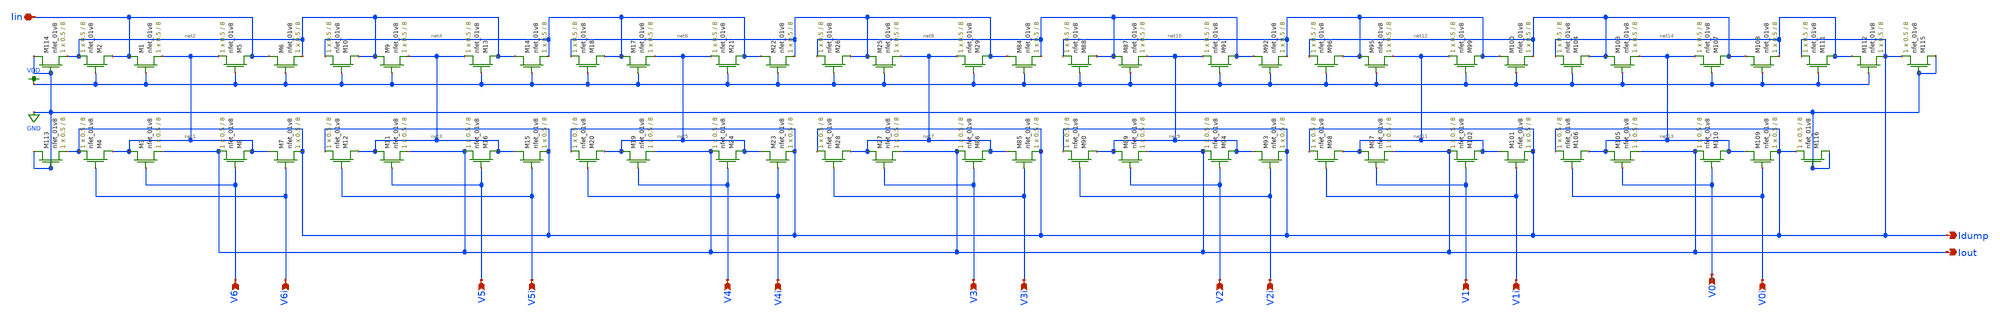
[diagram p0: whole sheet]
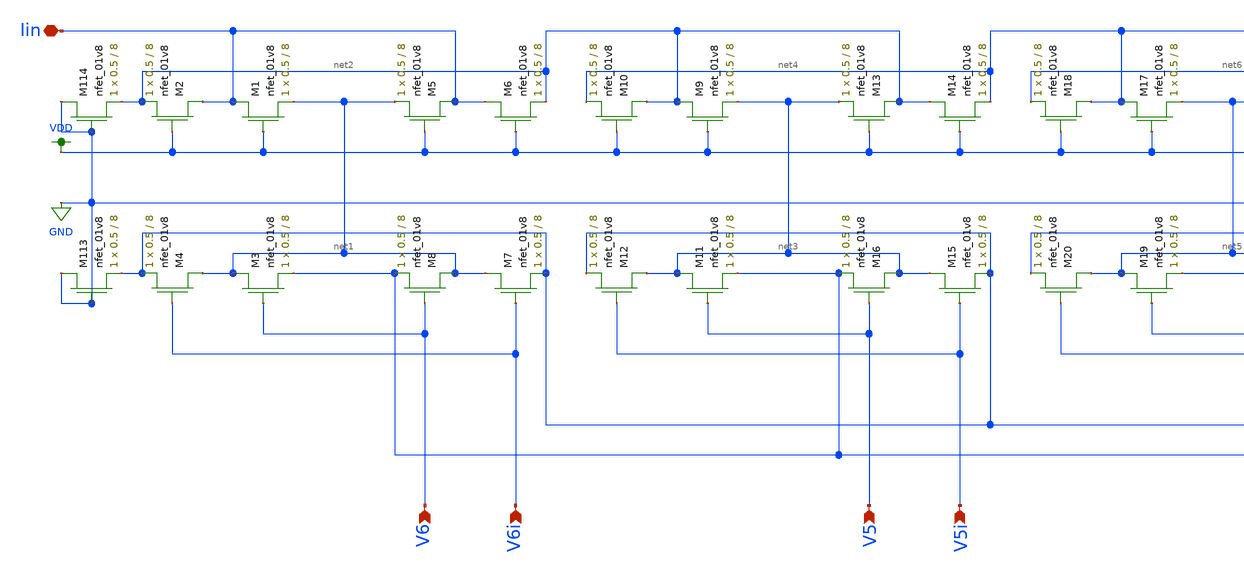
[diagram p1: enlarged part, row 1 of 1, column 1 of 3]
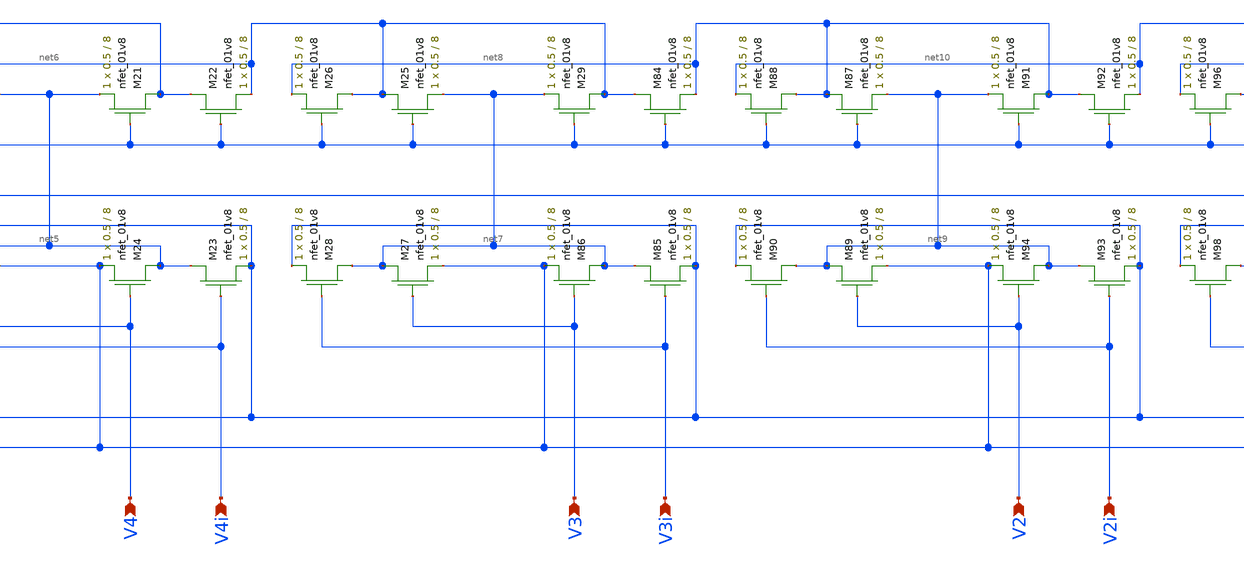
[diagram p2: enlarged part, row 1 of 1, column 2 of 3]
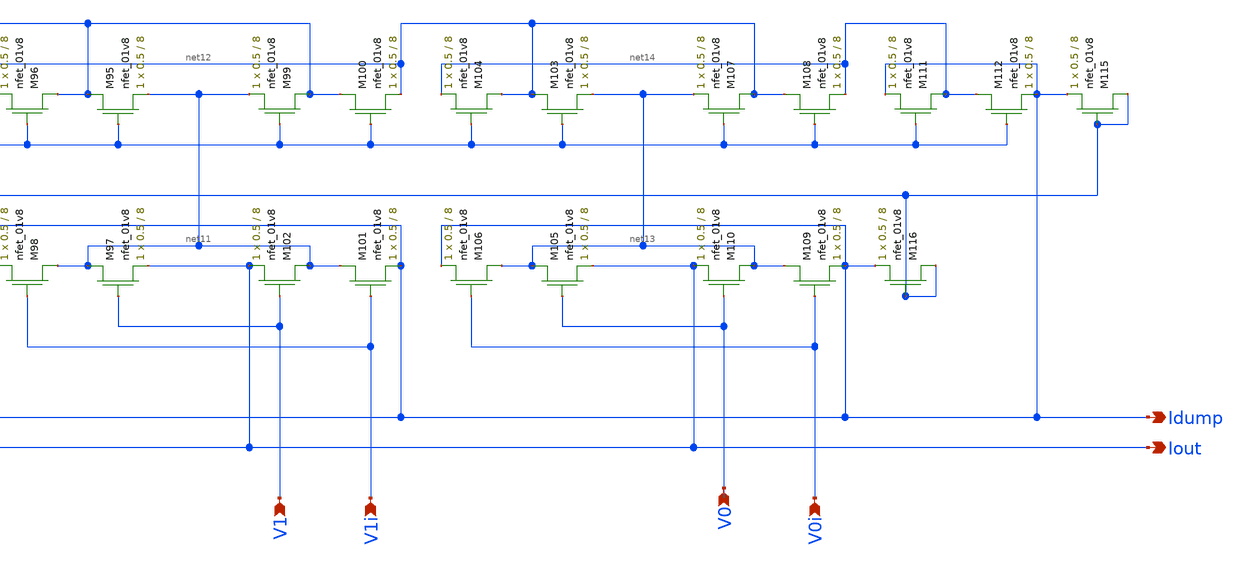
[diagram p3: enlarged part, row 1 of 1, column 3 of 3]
** sch_path: final-final-all/xschem/lds-ladder.sch
**.subckt lds-ladder Iin Idump Iout V6i V5i V4i V3i V2i V1i V0i V6 V5 V4 V3 V2 V1 V0
*.iopin Iin
*.opin Idump
*.opin Iout
*.ipin V6i
*.ipin V5i
*.ipin V4i
*.ipin V3i
*.ipin V2i
*.ipin V1i
*.ipin V0i
*.ipin V6
*.ipin V5
*.ipin V4
*.ipin V3
*.ipin V2
*.ipin V1
*.ipin V0
XM1 Iin VDD net1 GND sky130_fd_pr__nfet_01v8 L=8 W=0.5 nf=1 ad='int((nf+1)/2) * W/nf * 0.29' as='int((nf+2)/2) * W/nf * 0.29'
+ pd='2*int((nf+1)/2) * (W/nf + 0.29)' ps='2*int((nf+2)/2) * (W/nf + 0.29)' nrd='0.29 / W' nrs='0.29 / W'
+ sa=0 sb=0 sd=0 mult=1 m=1
XM2 Iin VDD net2 GND sky130_fd_pr__nfet_01v8 L=8 W=0.5 nf=1 ad='int((nf+1)/2) * W/nf * 0.29' as='int((nf+2)/2) * W/nf * 0.29'
+ pd='2*int((nf+1)/2) * (W/nf + 0.29)' ps='2*int((nf+2)/2) * (W/nf + 0.29)' nrd='0.29 / W' nrs='0.29 / W'
+ sa=0 sb=0 sd=0 mult=1 m=1
XM3 net1 V6 Iout GND sky130_fd_pr__nfet_01v8 L=8 W=0.5 nf=1 ad='int((nf+1)/2) * W/nf * 0.29' as='int((nf+2)/2) * W/nf * 0.29'
+ pd='2*int((nf+1)/2) * (W/nf + 0.29)' ps='2*int((nf+2)/2) * (W/nf + 0.29)' nrd='0.29 / W' nrs='0.29 / W'
+ sa=0 sb=0 sd=0 mult=1 m=1
XM4 net1 V6i Idump GND sky130_fd_pr__nfet_01v8 L=8 W=0.5 nf=1 ad='int((nf+1)/2) * W/nf * 0.29' as='int((nf+2)/2) * W/nf * 0.29'
+ pd='2*int((nf+1)/2) * (W/nf + 0.29)' ps='2*int((nf+2)/2) * (W/nf + 0.29)' nrd='0.29 / W' nrs='0.29 / W'
+ sa=0 sb=0 sd=0 mult=1 m=1
XM5 Iin VDD net1 GND sky130_fd_pr__nfet_01v8 L=8 W=0.5 nf=1 ad='int((nf+1)/2) * W/nf * 0.29' as='int((nf+2)/2) * W/nf * 0.29'
+ pd='2*int((nf+1)/2) * (W/nf + 0.29)' ps='2*int((nf+2)/2) * (W/nf + 0.29)' nrd='0.29 / W' nrs='0.29 / W'
+ sa=0 sb=0 sd=0 mult=1 m=1
XM6 Iin VDD net2 GND sky130_fd_pr__nfet_01v8 L=8 W=0.5 nf=1 ad='int((nf+1)/2) * W/nf * 0.29' as='int((nf+2)/2) * W/nf * 0.29'
+ pd='2*int((nf+1)/2) * (W/nf + 0.29)' ps='2*int((nf+2)/2) * (W/nf + 0.29)' nrd='0.29 / W' nrs='0.29 / W'
+ sa=0 sb=0 sd=0 mult=1 m=1
XM7 net1 V6i Idump GND sky130_fd_pr__nfet_01v8 L=8 W=0.5 nf=1 ad='int((nf+1)/2) * W/nf * 0.29' as='int((nf+2)/2) * W/nf * 0.29'
+ pd='2*int((nf+1)/2) * (W/nf + 0.29)' ps='2*int((nf+2)/2) * (W/nf + 0.29)' nrd='0.29 / W' nrs='0.29 / W'
+ sa=0 sb=0 sd=0 mult=1 m=1
XM8 net1 V6 Iout GND sky130_fd_pr__nfet_01v8 L=8 W=0.5 nf=1 ad='int((nf+1)/2) * W/nf * 0.29' as='int((nf+2)/2) * W/nf * 0.29'
+ pd='2*int((nf+1)/2) * (W/nf + 0.29)' ps='2*int((nf+2)/2) * (W/nf + 0.29)' nrd='0.29 / W' nrs='0.29 / W'
+ sa=0 sb=0 sd=0 mult=1 m=1
XM9 net2 VDD net3 GND sky130_fd_pr__nfet_01v8 L=8 W=0.5 nf=1 ad='int((nf+1)/2) * W/nf * 0.29' as='int((nf+2)/2) * W/nf * 0.29'
+ pd='2*int((nf+1)/2) * (W/nf + 0.29)' ps='2*int((nf+2)/2) * (W/nf + 0.29)' nrd='0.29 / W' nrs='0.29 / W'
+ sa=0 sb=0 sd=0 mult=1 m=1
XM10 net2 VDD net4 GND sky130_fd_pr__nfet_01v8 L=8 W=0.5 nf=1 ad='int((nf+1)/2) * W/nf * 0.29' as='int((nf+2)/2) * W/nf * 0.29'
+ pd='2*int((nf+1)/2) * (W/nf + 0.29)' ps='2*int((nf+2)/2) * (W/nf + 0.29)' nrd='0.29 / W' nrs='0.29 / W'
+ sa=0 sb=0 sd=0 mult=1 m=1
XM11 net3 V5 Iout GND sky130_fd_pr__nfet_01v8 L=8 W=0.5 nf=1 ad='int((nf+1)/2) * W/nf * 0.29' as='int((nf+2)/2) * W/nf * 0.29'
+ pd='2*int((nf+1)/2) * (W/nf + 0.29)' ps='2*int((nf+2)/2) * (W/nf + 0.29)' nrd='0.29 / W' nrs='0.29 / W'
+ sa=0 sb=0 sd=0 mult=1 m=1
XM12 net3 V5i Idump GND sky130_fd_pr__nfet_01v8 L=8 W=0.5 nf=1 ad='int((nf+1)/2) * W/nf * 0.29' as='int((nf+2)/2) * W/nf * 0.29'
+ pd='2*int((nf+1)/2) * (W/nf + 0.29)' ps='2*int((nf+2)/2) * (W/nf + 0.29)' nrd='0.29 / W' nrs='0.29 / W'
+ sa=0 sb=0 sd=0 mult=1 m=1
XM13 net2 VDD net3 GND sky130_fd_pr__nfet_01v8 L=8 W=0.5 nf=1 ad='int((nf+1)/2) * W/nf * 0.29' as='int((nf+2)/2) * W/nf * 0.29'
+ pd='2*int((nf+1)/2) * (W/nf + 0.29)' ps='2*int((nf+2)/2) * (W/nf + 0.29)' nrd='0.29 / W' nrs='0.29 / W'
+ sa=0 sb=0 sd=0 mult=1 m=1
XM14 net2 VDD net4 GND sky130_fd_pr__nfet_01v8 L=8 W=0.5 nf=1 ad='int((nf+1)/2) * W/nf * 0.29' as='int((nf+2)/2) * W/nf * 0.29'
+ pd='2*int((nf+1)/2) * (W/nf + 0.29)' ps='2*int((nf+2)/2) * (W/nf + 0.29)' nrd='0.29 / W' nrs='0.29 / W'
+ sa=0 sb=0 sd=0 mult=1 m=1
XM15 net3 V5i Idump GND sky130_fd_pr__nfet_01v8 L=8 W=0.5 nf=1 ad='int((nf+1)/2) * W/nf * 0.29' as='int((nf+2)/2) * W/nf * 0.29'
+ pd='2*int((nf+1)/2) * (W/nf + 0.29)' ps='2*int((nf+2)/2) * (W/nf + 0.29)' nrd='0.29 / W' nrs='0.29 / W'
+ sa=0 sb=0 sd=0 mult=1 m=1
XM16 net3 V5 Iout GND sky130_fd_pr__nfet_01v8 L=8 W=0.5 nf=1 ad='int((nf+1)/2) * W/nf * 0.29' as='int((nf+2)/2) * W/nf * 0.29'
+ pd='2*int((nf+1)/2) * (W/nf + 0.29)' ps='2*int((nf+2)/2) * (W/nf + 0.29)' nrd='0.29 / W' nrs='0.29 / W'
+ sa=0 sb=0 sd=0 mult=1 m=1
XM17 net4 VDD net5 GND sky130_fd_pr__nfet_01v8 L=8 W=0.5 nf=1 ad='int((nf+1)/2) * W/nf * 0.29' as='int((nf+2)/2) * W/nf * 0.29'
+ pd='2*int((nf+1)/2) * (W/nf + 0.29)' ps='2*int((nf+2)/2) * (W/nf + 0.29)' nrd='0.29 / W' nrs='0.29 / W'
+ sa=0 sb=0 sd=0 mult=1 m=1
XM18 net4 VDD net6 GND sky130_fd_pr__nfet_01v8 L=8 W=0.5 nf=1 ad='int((nf+1)/2) * W/nf * 0.29' as='int((nf+2)/2) * W/nf * 0.29'
+ pd='2*int((nf+1)/2) * (W/nf + 0.29)' ps='2*int((nf+2)/2) * (W/nf + 0.29)' nrd='0.29 / W' nrs='0.29 / W'
+ sa=0 sb=0 sd=0 mult=1 m=1
XM19 net5 V4 Iout GND sky130_fd_pr__nfet_01v8 L=8 W=0.5 nf=1 ad='int((nf+1)/2) * W/nf * 0.29' as='int((nf+2)/2) * W/nf * 0.29'
+ pd='2*int((nf+1)/2) * (W/nf + 0.29)' ps='2*int((nf+2)/2) * (W/nf + 0.29)' nrd='0.29 / W' nrs='0.29 / W'
+ sa=0 sb=0 sd=0 mult=1 m=1
XM20 net5 V4i Idump GND sky130_fd_pr__nfet_01v8 L=8 W=0.5 nf=1 ad='int((nf+1)/2) * W/nf * 0.29' as='int((nf+2)/2) * W/nf * 0.29'
+ pd='2*int((nf+1)/2) * (W/nf + 0.29)' ps='2*int((nf+2)/2) * (W/nf + 0.29)' nrd='0.29 / W' nrs='0.29 / W'
+ sa=0 sb=0 sd=0 mult=1 m=1
XM21 net4 VDD net5 GND sky130_fd_pr__nfet_01v8 L=8 W=0.5 nf=1 ad='int((nf+1)/2) * W/nf * 0.29' as='int((nf+2)/2) * W/nf * 0.29'
+ pd='2*int((nf+1)/2) * (W/nf + 0.29)' ps='2*int((nf+2)/2) * (W/nf + 0.29)' nrd='0.29 / W' nrs='0.29 / W'
+ sa=0 sb=0 sd=0 mult=1 m=1
XM22 net4 VDD net6 GND sky130_fd_pr__nfet_01v8 L=8 W=0.5 nf=1 ad='int((nf+1)/2) * W/nf * 0.29' as='int((nf+2)/2) * W/nf * 0.29'
+ pd='2*int((nf+1)/2) * (W/nf + 0.29)' ps='2*int((nf+2)/2) * (W/nf + 0.29)' nrd='0.29 / W' nrs='0.29 / W'
+ sa=0 sb=0 sd=0 mult=1 m=1
XM23 net5 V4i Idump GND sky130_fd_pr__nfet_01v8 L=8 W=0.5 nf=1 ad='int((nf+1)/2) * W/nf * 0.29' as='int((nf+2)/2) * W/nf * 0.29'
+ pd='2*int((nf+1)/2) * (W/nf + 0.29)' ps='2*int((nf+2)/2) * (W/nf + 0.29)' nrd='0.29 / W' nrs='0.29 / W'
+ sa=0 sb=0 sd=0 mult=1 m=1
XM24 net5 V4 Iout GND sky130_fd_pr__nfet_01v8 L=8 W=0.5 nf=1 ad='int((nf+1)/2) * W/nf * 0.29' as='int((nf+2)/2) * W/nf * 0.29'
+ pd='2*int((nf+1)/2) * (W/nf + 0.29)' ps='2*int((nf+2)/2) * (W/nf + 0.29)' nrd='0.29 / W' nrs='0.29 / W'
+ sa=0 sb=0 sd=0 mult=1 m=1
XM25 net6 VDD net7 GND sky130_fd_pr__nfet_01v8 L=8 W=0.5 nf=1 ad='int((nf+1)/2) * W/nf * 0.29' as='int((nf+2)/2) * W/nf * 0.29'
+ pd='2*int((nf+1)/2) * (W/nf + 0.29)' ps='2*int((nf+2)/2) * (W/nf + 0.29)' nrd='0.29 / W' nrs='0.29 / W'
+ sa=0 sb=0 sd=0 mult=1 m=1
XM26 net6 VDD net8 GND sky130_fd_pr__nfet_01v8 L=8 W=0.5 nf=1 ad='int((nf+1)/2) * W/nf * 0.29' as='int((nf+2)/2) * W/nf * 0.29'
+ pd='2*int((nf+1)/2) * (W/nf + 0.29)' ps='2*int((nf+2)/2) * (W/nf + 0.29)' nrd='0.29 / W' nrs='0.29 / W'
+ sa=0 sb=0 sd=0 mult=1 m=1
XM27 net7 V3 Iout GND sky130_fd_pr__nfet_01v8 L=8 W=0.5 nf=1 ad='int((nf+1)/2) * W/nf * 0.29' as='int((nf+2)/2) * W/nf * 0.29'
+ pd='2*int((nf+1)/2) * (W/nf + 0.29)' ps='2*int((nf+2)/2) * (W/nf + 0.29)' nrd='0.29 / W' nrs='0.29 / W'
+ sa=0 sb=0 sd=0 mult=1 m=1
XM28 net7 V3i Idump GND sky130_fd_pr__nfet_01v8 L=8 W=0.5 nf=1 ad='int((nf+1)/2) * W/nf * 0.29' as='int((nf+2)/2) * W/nf * 0.29'
+ pd='2*int((nf+1)/2) * (W/nf + 0.29)' ps='2*int((nf+2)/2) * (W/nf + 0.29)' nrd='0.29 / W' nrs='0.29 / W'
+ sa=0 sb=0 sd=0 mult=1 m=1
XM29 net6 VDD net7 GND sky130_fd_pr__nfet_01v8 L=8 W=0.5 nf=1 ad='int((nf+1)/2) * W/nf * 0.29' as='int((nf+2)/2) * W/nf * 0.29'
+ pd='2*int((nf+1)/2) * (W/nf + 0.29)' ps='2*int((nf+2)/2) * (W/nf + 0.29)' nrd='0.29 / W' nrs='0.29 / W'
+ sa=0 sb=0 sd=0 mult=1 m=1
XM84 net6 VDD net8 GND sky130_fd_pr__nfet_01v8 L=8 W=0.5 nf=1 ad='int((nf+1)/2) * W/nf * 0.29' as='int((nf+2)/2) * W/nf * 0.29'
+ pd='2*int((nf+1)/2) * (W/nf + 0.29)' ps='2*int((nf+2)/2) * (W/nf + 0.29)' nrd='0.29 / W' nrs='0.29 / W'
+ sa=0 sb=0 sd=0 mult=1 m=1
XM85 net7 V3i Idump GND sky130_fd_pr__nfet_01v8 L=8 W=0.5 nf=1 ad='int((nf+1)/2) * W/nf * 0.29' as='int((nf+2)/2) * W/nf * 0.29'
+ pd='2*int((nf+1)/2) * (W/nf + 0.29)' ps='2*int((nf+2)/2) * (W/nf + 0.29)' nrd='0.29 / W' nrs='0.29 / W'
+ sa=0 sb=0 sd=0 mult=1 m=1
XM86 net7 V3 Iout GND sky130_fd_pr__nfet_01v8 L=8 W=0.5 nf=1 ad='int((nf+1)/2) * W/nf * 0.29' as='int((nf+2)/2) * W/nf * 0.29'
+ pd='2*int((nf+1)/2) * (W/nf + 0.29)' ps='2*int((nf+2)/2) * (W/nf + 0.29)' nrd='0.29 / W' nrs='0.29 / W'
+ sa=0 sb=0 sd=0 mult=1 m=1
XM87 net8 VDD net9 GND sky130_fd_pr__nfet_01v8 L=8 W=0.5 nf=1 ad='int((nf+1)/2) * W/nf * 0.29' as='int((nf+2)/2) * W/nf * 0.29'
+ pd='2*int((nf+1)/2) * (W/nf + 0.29)' ps='2*int((nf+2)/2) * (W/nf + 0.29)' nrd='0.29 / W' nrs='0.29 / W'
+ sa=0 sb=0 sd=0 mult=1 m=1
XM88 net8 VDD net10 GND sky130_fd_pr__nfet_01v8 L=8 W=0.5 nf=1 ad='int((nf+1)/2) * W/nf * 0.29' as='int((nf+2)/2) * W/nf * 0.29'
+ pd='2*int((nf+1)/2) * (W/nf + 0.29)' ps='2*int((nf+2)/2) * (W/nf + 0.29)' nrd='0.29 / W' nrs='0.29 / W'
+ sa=0 sb=0 sd=0 mult=1 m=1
XM89 net9 V2 Iout GND sky130_fd_pr__nfet_01v8 L=8 W=0.5 nf=1 ad='int((nf+1)/2) * W/nf * 0.29' as='int((nf+2)/2) * W/nf * 0.29'
+ pd='2*int((nf+1)/2) * (W/nf + 0.29)' ps='2*int((nf+2)/2) * (W/nf + 0.29)' nrd='0.29 / W' nrs='0.29 / W'
+ sa=0 sb=0 sd=0 mult=1 m=1
XM90 net9 V2i Idump GND sky130_fd_pr__nfet_01v8 L=8 W=0.5 nf=1 ad='int((nf+1)/2) * W/nf * 0.29' as='int((nf+2)/2) * W/nf * 0.29'
+ pd='2*int((nf+1)/2) * (W/nf + 0.29)' ps='2*int((nf+2)/2) * (W/nf + 0.29)' nrd='0.29 / W' nrs='0.29 / W'
+ sa=0 sb=0 sd=0 mult=1 m=1
XM91 net8 VDD net9 GND sky130_fd_pr__nfet_01v8 L=8 W=0.5 nf=1 ad='int((nf+1)/2) * W/nf * 0.29' as='int((nf+2)/2) * W/nf * 0.29'
+ pd='2*int((nf+1)/2) * (W/nf + 0.29)' ps='2*int((nf+2)/2) * (W/nf + 0.29)' nrd='0.29 / W' nrs='0.29 / W'
+ sa=0 sb=0 sd=0 mult=1 m=1
XM92 net8 VDD net10 GND sky130_fd_pr__nfet_01v8 L=8 W=0.5 nf=1 ad='int((nf+1)/2) * W/nf * 0.29' as='int((nf+2)/2) * W/nf * 0.29'
+ pd='2*int((nf+1)/2) * (W/nf + 0.29)' ps='2*int((nf+2)/2) * (W/nf + 0.29)' nrd='0.29 / W' nrs='0.29 / W'
+ sa=0 sb=0 sd=0 mult=1 m=1
XM93 net9 V2i Idump GND sky130_fd_pr__nfet_01v8 L=8 W=0.5 nf=1 ad='int((nf+1)/2) * W/nf * 0.29' as='int((nf+2)/2) * W/nf * 0.29'
+ pd='2*int((nf+1)/2) * (W/nf + 0.29)' ps='2*int((nf+2)/2) * (W/nf + 0.29)' nrd='0.29 / W' nrs='0.29 / W'
+ sa=0 sb=0 sd=0 mult=1 m=1
XM94 net9 V2 Iout GND sky130_fd_pr__nfet_01v8 L=8 W=0.5 nf=1 ad='int((nf+1)/2) * W/nf * 0.29' as='int((nf+2)/2) * W/nf * 0.29'
+ pd='2*int((nf+1)/2) * (W/nf + 0.29)' ps='2*int((nf+2)/2) * (W/nf + 0.29)' nrd='0.29 / W' nrs='0.29 / W'
+ sa=0 sb=0 sd=0 mult=1 m=1
XM95 net10 VDD net11 GND sky130_fd_pr__nfet_01v8 L=8 W=0.5 nf=1 ad='int((nf+1)/2) * W/nf * 0.29' as='int((nf+2)/2) * W/nf * 0.29'
+ pd='2*int((nf+1)/2) * (W/nf + 0.29)' ps='2*int((nf+2)/2) * (W/nf + 0.29)' nrd='0.29 / W' nrs='0.29 / W'
+ sa=0 sb=0 sd=0 mult=1 m=1
XM96 net10 VDD net12 GND sky130_fd_pr__nfet_01v8 L=8 W=0.5 nf=1 ad='int((nf+1)/2) * W/nf * 0.29' as='int((nf+2)/2) * W/nf * 0.29'
+ pd='2*int((nf+1)/2) * (W/nf + 0.29)' ps='2*int((nf+2)/2) * (W/nf + 0.29)' nrd='0.29 / W' nrs='0.29 / W'
+ sa=0 sb=0 sd=0 mult=1 m=1
XM97 net11 V1 Iout GND sky130_fd_pr__nfet_01v8 L=8 W=0.5 nf=1 ad='int((nf+1)/2) * W/nf * 0.29' as='int((nf+2)/2) * W/nf * 0.29'
+ pd='2*int((nf+1)/2) * (W/nf + 0.29)' ps='2*int((nf+2)/2) * (W/nf + 0.29)' nrd='0.29 / W' nrs='0.29 / W'
+ sa=0 sb=0 sd=0 mult=1 m=1
XM98 net11 V1i Idump GND sky130_fd_pr__nfet_01v8 L=8 W=0.5 nf=1 ad='int((nf+1)/2) * W/nf * 0.29' as='int((nf+2)/2) * W/nf * 0.29'
+ pd='2*int((nf+1)/2) * (W/nf + 0.29)' ps='2*int((nf+2)/2) * (W/nf + 0.29)' nrd='0.29 / W' nrs='0.29 / W'
+ sa=0 sb=0 sd=0 mult=1 m=1
XM99 net10 VDD net11 GND sky130_fd_pr__nfet_01v8 L=8 W=0.5 nf=1 ad='int((nf+1)/2) * W/nf * 0.29' as='int((nf+2)/2) * W/nf * 0.29'
+ pd='2*int((nf+1)/2) * (W/nf + 0.29)' ps='2*int((nf+2)/2) * (W/nf + 0.29)' nrd='0.29 / W' nrs='0.29 / W'
+ sa=0 sb=0 sd=0 mult=1 m=1
XM100 net10 VDD net12 GND sky130_fd_pr__nfet_01v8 L=8 W=0.5 nf=1 ad='int((nf+1)/2) * W/nf * 0.29' as='int((nf+2)/2) * W/nf * 0.29'
+ pd='2*int((nf+1)/2) * (W/nf + 0.29)' ps='2*int((nf+2)/2) * (W/nf + 0.29)' nrd='0.29 / W' nrs='0.29 / W'
+ sa=0 sb=0 sd=0 mult=1 m=1
XM101 net11 V1i Idump GND sky130_fd_pr__nfet_01v8 L=8 W=0.5 nf=1 ad='int((nf+1)/2) * W/nf * 0.29' as='int((nf+2)/2) * W/nf * 0.29'
+ pd='2*int((nf+1)/2) * (W/nf + 0.29)' ps='2*int((nf+2)/2) * (W/nf + 0.29)' nrd='0.29 / W' nrs='0.29 / W'
+ sa=0 sb=0 sd=0 mult=1 m=1
XM102 net11 V1 Iout GND sky130_fd_pr__nfet_01v8 L=8 W=0.5 nf=1 ad='int((nf+1)/2) * W/nf * 0.29' as='int((nf+2)/2) * W/nf * 0.29'
+ pd='2*int((nf+1)/2) * (W/nf + 0.29)' ps='2*int((nf+2)/2) * (W/nf + 0.29)' nrd='0.29 / W' nrs='0.29 / W'
+ sa=0 sb=0 sd=0 mult=1 m=1
XM103 net12 VDD net13 GND sky130_fd_pr__nfet_01v8 L=8 W=0.5 nf=1 ad='int((nf+1)/2) * W/nf * 0.29' as='int((nf+2)/2) * W/nf * 0.29'
+ pd='2*int((nf+1)/2) * (W/nf + 0.29)' ps='2*int((nf+2)/2) * (W/nf + 0.29)' nrd='0.29 / W' nrs='0.29 / W'
+ sa=0 sb=0 sd=0 mult=1 m=1
XM104 net12 VDD net14 GND sky130_fd_pr__nfet_01v8 L=8 W=0.5 nf=1 ad='int((nf+1)/2) * W/nf * 0.29' as='int((nf+2)/2) * W/nf * 0.29'
+ pd='2*int((nf+1)/2) * (W/nf + 0.29)' ps='2*int((nf+2)/2) * (W/nf + 0.29)' nrd='0.29 / W' nrs='0.29 / W'
+ sa=0 sb=0 sd=0 mult=1 m=1
XM105 net13 V0 Iout GND sky130_fd_pr__nfet_01v8 L=8 W=0.5 nf=1 ad='int((nf+1)/2) * W/nf * 0.29' as='int((nf+2)/2) * W/nf * 0.29'
+ pd='2*int((nf+1)/2) * (W/nf + 0.29)' ps='2*int((nf+2)/2) * (W/nf + 0.29)' nrd='0.29 / W' nrs='0.29 / W'
+ sa=0 sb=0 sd=0 mult=1 m=1
XM106 net13 V0i Idump GND sky130_fd_pr__nfet_01v8 L=8 W=0.5 nf=1 ad='int((nf+1)/2) * W/nf * 0.29' as='int((nf+2)/2) * W/nf * 0.29'
+ pd='2*int((nf+1)/2) * (W/nf + 0.29)' ps='2*int((nf+2)/2) * (W/nf + 0.29)' nrd='0.29 / W' nrs='0.29 / W'
+ sa=0 sb=0 sd=0 mult=1 m=1
XM107 net12 VDD net13 GND sky130_fd_pr__nfet_01v8 L=8 W=0.5 nf=1 ad='int((nf+1)/2) * W/nf * 0.29' as='int((nf+2)/2) * W/nf * 0.29'
+ pd='2*int((nf+1)/2) * (W/nf + 0.29)' ps='2*int((nf+2)/2) * (W/nf + 0.29)' nrd='0.29 / W' nrs='0.29 / W'
+ sa=0 sb=0 sd=0 mult=1 m=1
XM108 net12 VDD net14 GND sky130_fd_pr__nfet_01v8 L=8 W=0.5 nf=1 ad='int((nf+1)/2) * W/nf * 0.29' as='int((nf+2)/2) * W/nf * 0.29'
+ pd='2*int((nf+1)/2) * (W/nf + 0.29)' ps='2*int((nf+2)/2) * (W/nf + 0.29)' nrd='0.29 / W' nrs='0.29 / W'
+ sa=0 sb=0 sd=0 mult=1 m=1
XM109 net13 V0i Idump GND sky130_fd_pr__nfet_01v8 L=8 W=0.5 nf=1 ad='int((nf+1)/2) * W/nf * 0.29' as='int((nf+2)/2) * W/nf * 0.29'
+ pd='2*int((nf+1)/2) * (W/nf + 0.29)' ps='2*int((nf+2)/2) * (W/nf + 0.29)' nrd='0.29 / W' nrs='0.29 / W'
+ sa=0 sb=0 sd=0 mult=1 m=1
XM110 net13 V0 Iout GND sky130_fd_pr__nfet_01v8 L=8 W=0.5 nf=1 ad='int((nf+1)/2) * W/nf * 0.29' as='int((nf+2)/2) * W/nf * 0.29'
+ pd='2*int((nf+1)/2) * (W/nf + 0.29)' ps='2*int((nf+2)/2) * (W/nf + 0.29)' nrd='0.29 / W' nrs='0.29 / W'
+ sa=0 sb=0 sd=0 mult=1 m=1
XM111 net14 VDD Idump GND sky130_fd_pr__nfet_01v8 L=8 W=0.5 nf=1 ad='int((nf+1)/2) * W/nf * 0.29' as='int((nf+2)/2) * W/nf * 0.29'
+ pd='2*int((nf+1)/2) * (W/nf + 0.29)' ps='2*int((nf+2)/2) * (W/nf + 0.29)' nrd='0.29 / W' nrs='0.29 / W'
+ sa=0 sb=0 sd=0 mult=1 m=1
XM112 net14 VDD Idump GND sky130_fd_pr__nfet_01v8 L=8 W=0.5 nf=1 ad='int((nf+1)/2) * W/nf * 0.29' as='int((nf+2)/2) * W/nf * 0.29'
+ pd='2*int((nf+1)/2) * (W/nf + 0.29)' ps='2*int((nf+2)/2) * (W/nf + 0.29)' nrd='0.29 / W' nrs='0.29 / W'
+ sa=0 sb=0 sd=0 mult=1 m=1
XM113 GND GND Idump GND sky130_fd_pr__nfet_01v8 L=8 W=0.5 nf=1 ad='int((nf+1)/2) * W/nf * 0.29' as='int((nf+2)/2) * W/nf * 0.29'
+ pd='2*int((nf+1)/2) * (W/nf + 0.29)' ps='2*int((nf+2)/2) * (W/nf + 0.29)' nrd='0.29 / W' nrs='0.29 / W'
+ sa=0 sb=0 sd=0 mult=1 m=1
XM114 GND GND net2 GND sky130_fd_pr__nfet_01v8 L=8 W=0.5 nf=1 ad='int((nf+1)/2) * W/nf * 0.29' as='int((nf+2)/2) * W/nf * 0.29'
+ pd='2*int((nf+1)/2) * (W/nf + 0.29)' ps='2*int((nf+2)/2) * (W/nf + 0.29)' nrd='0.29 / W' nrs='0.29 / W'
+ sa=0 sb=0 sd=0 mult=1 m=1
XM115 GND GND Idump GND sky130_fd_pr__nfet_01v8 L=8 W=0.5 nf=1 ad='int((nf+1)/2) * W/nf * 0.29' as='int((nf+2)/2) * W/nf * 0.29'
+ pd='2*int((nf+1)/2) * (W/nf + 0.29)' ps='2*int((nf+2)/2) * (W/nf + 0.29)' nrd='0.29 / W' nrs='0.29 / W'
+ sa=0 sb=0 sd=0 mult=1 m=1
XM116 GND GND Idump GND sky130_fd_pr__nfet_01v8 L=8 W=0.5 nf=1 ad='int((nf+1)/2) * W/nf * 0.29' as='int((nf+2)/2) * W/nf * 0.29'
+ pd='2*int((nf+1)/2) * (W/nf + 0.29)' ps='2*int((nf+2)/2) * (W/nf + 0.29)' nrd='0.29 / W' nrs='0.29 / W'
+ sa=0 sb=0 sd=0 mult=1 m=1
**.ends
.GLOBAL VDD
.GLOBAL GND
.end
